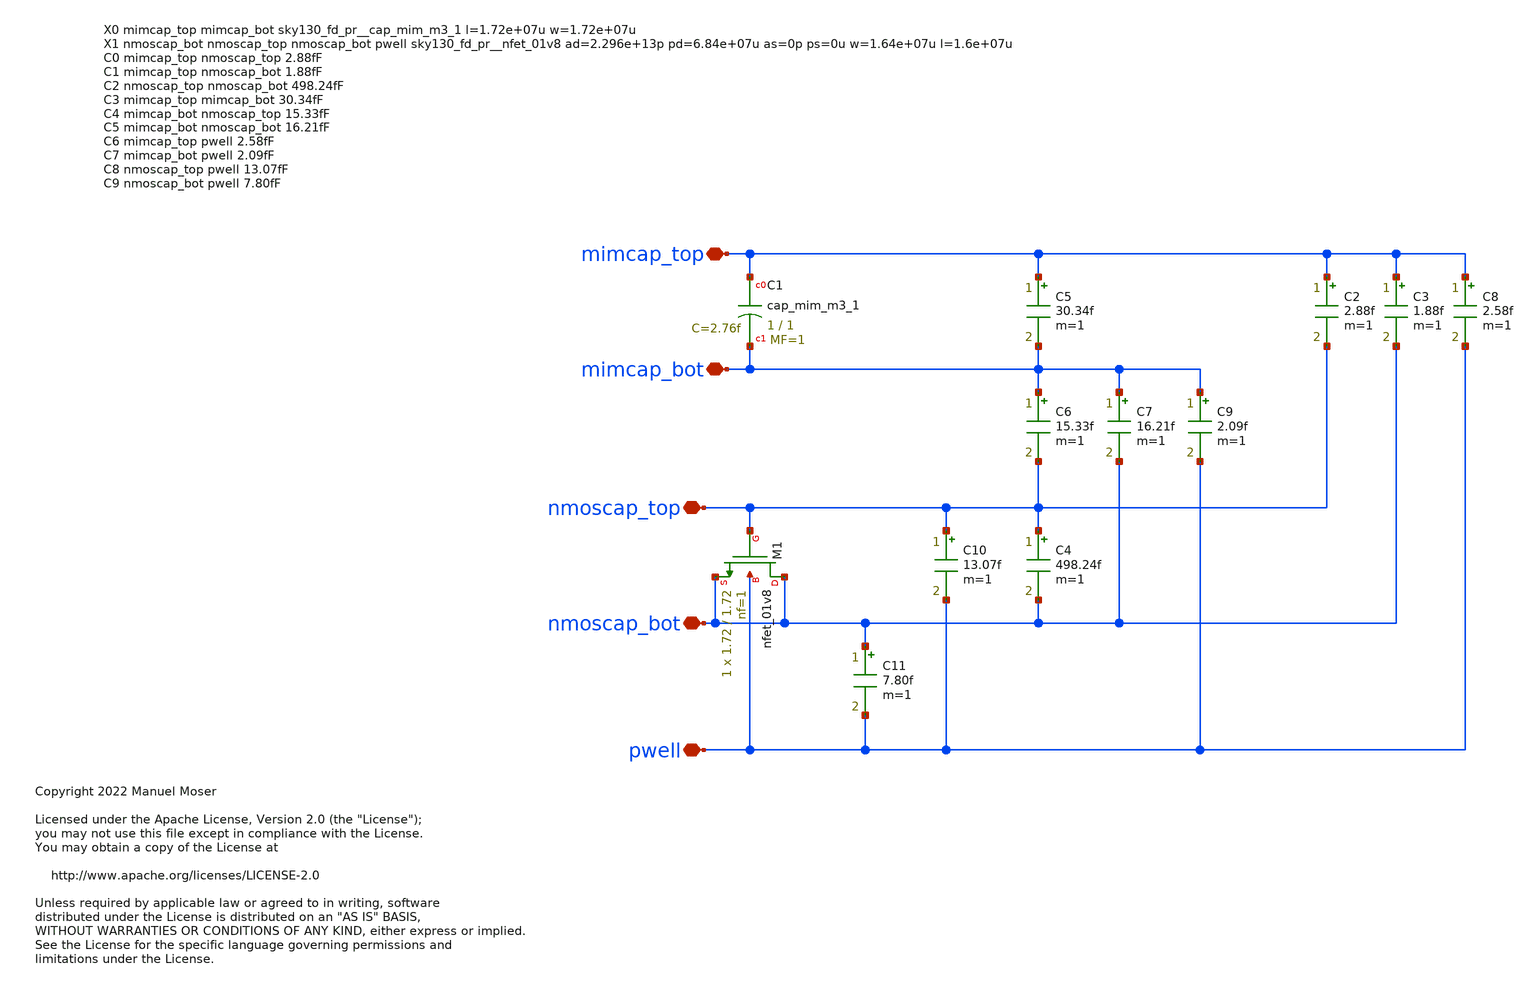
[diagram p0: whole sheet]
** sch_path: xschem/adc_noise_decoup_cell/adc_noise_decoup_cell1_parasiticcs.sch
* Copyright 2022 Manuel Moser
* Licensed under the Apache License, Version 2.0 (the "License");
**.subckt adc_noise_decoup_cell1_parasiticcs nmoscap_top mimcap_top mimcap_bot nmoscap_bot pwell
*.iopin nmoscap_top
*.iopin mimcap_top
*.iopin mimcap_bot
*.iopin nmoscap_bot
*.iopin pwell
XC1 mimcap_top mimcap_bot sky130_fd_pr__cap_mim_m3_1 W=1 L=1 MF=1 m=1
XM1 nmoscap_bot nmoscap_top nmoscap_bot pwell sky130_fd_pr__nfet_01v8 L=1.72 W=1.72 nf=1 ad='int((nf+1)/2) * W/nf * 0.29'
+ as='int((nf+2)/2) * W/nf * 0.29' pd='2*int((nf+1)/2) * (W/nf + 0.29)' ps='2*int((nf+2)/2) * (W/nf + 0.29)'
+ nrd='0.29 / W' nrs='0.29 / W' sa=0 sb=0 sd=0 mult=1 m=1
C2 mimcap_top nmoscap_top 2.88f m=1
C3 mimcap_top nmoscap_bot 1.88f m=1
C4 nmoscap_top nmoscap_bot 498.24f m=1
C5 mimcap_top mimcap_bot 30.34f m=1
C6 mimcap_bot nmoscap_top 15.33f m=1
C7 mimcap_bot nmoscap_bot 16.21f m=1
C8 mimcap_top pwell 2.58f m=1
C9 mimcap_bot pwell 2.09f m=1
C10 nmoscap_top pwell 13.07f m=1
C11 nmoscap_bot pwell 7.80f m=1
**.ends
.end
